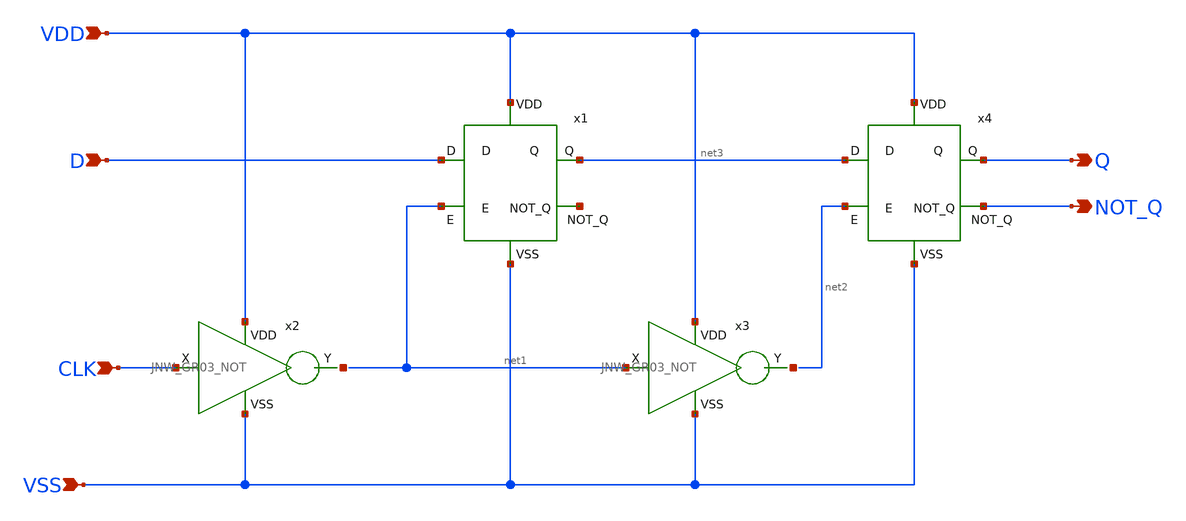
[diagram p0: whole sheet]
** sch_path: design/JNW_GR03_SKY130A/JNW_GR03_DFLIPFLOP_R.sch
**.subckt JNW_GR03_DFLIPFLOP_R VDD VSS D CLK Q NOT_Q
*.ipin VDD
*.ipin VSS
*.ipin D
*.ipin CLK
*.opin Q
*.opin NOT_Q
x1 VDD D net3 net4 net1 VSS JNW_GR03_DLATCH
x2 VDD CLK net5 VSS JNW_GR03_NOT
x3 VDD net1 net6 VSS JNW_GR03_NOT
x4 VDD net3 Q NOT_Q net2 VSS JNW_GR03_DLATCH
**.ends
.end
